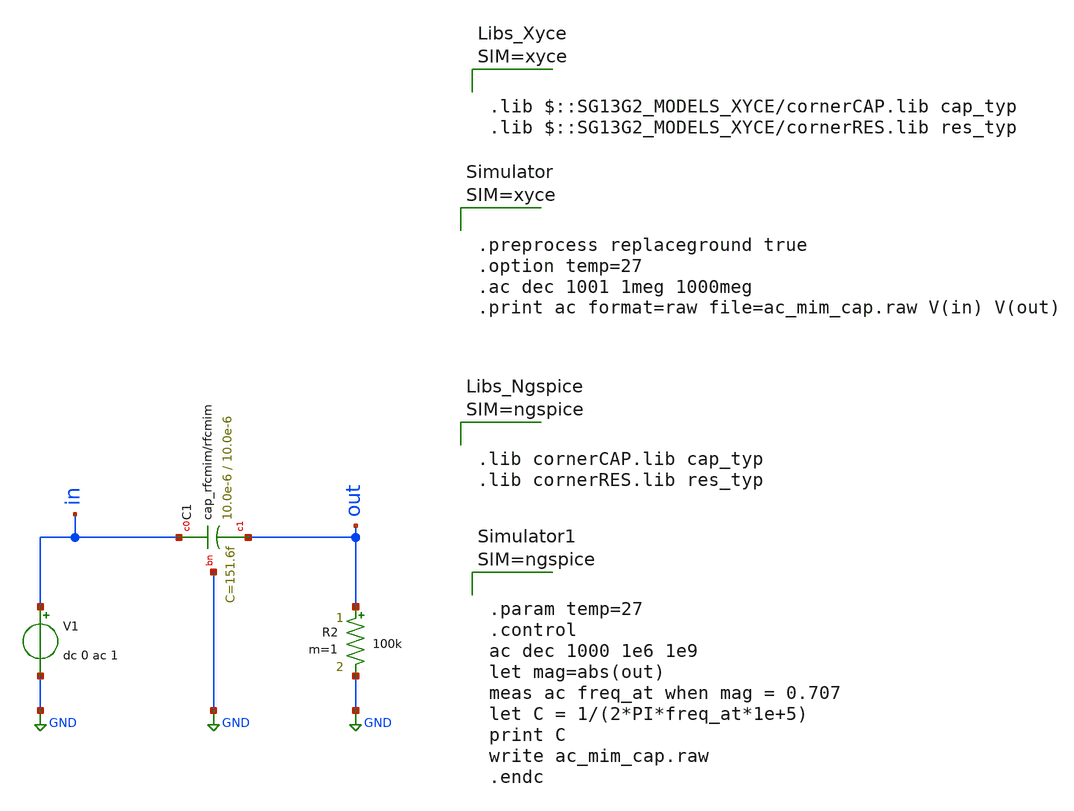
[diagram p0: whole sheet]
** sch_path: ihp-sg13g2/libs.tech/xschem/sg13g2_tests_xyce/ac_rfmim_cap.sch
* Copyright 2021 Stefan Frederik Schippers
* Licensed under the Apache License, Version 2.0 (the "License");
* you may not use this file except in compliance with the License.
* You may obtain a copy of the License at
* https://www.apache.org/licenses/LICENSE-2.0
* Unless required by applicable law or agreed to in writing, software
* distributed under the License is distributed on an "AS IS" BASIS,
* WITHOUT WARRANTIES OR CONDITIONS OF ANY KIND, either express or implied.
* See the License for the specific language governing permissions and
* limitations under the License.
* Copyright 2023 IHP PDK Authors
**.subckt ac_rfmim_cap
V1 in GND dc 0 ac 1
R2 out GND 100k m=1
XC1 in out GND cap_rfcmim w=10.0e-6 l=10.0e-6 wfeed=5.0e-6 m=1 mm_ok=1
**** begin user architecture code









.lib cornerCAP.lib cap_typ
.lib cornerRES.lib res_typ






.param temp=27
.control
ac dec 1000 1e6 1e9
let mag=abs(out)
meas ac freq_at when mag = 0.707
let C = 1/(2*PI*freq_at*1e+5)
print C
write ac_mim_cap.raw
.endc



**** end user architecture code
**.ends
.GLOBAL GND
.end
